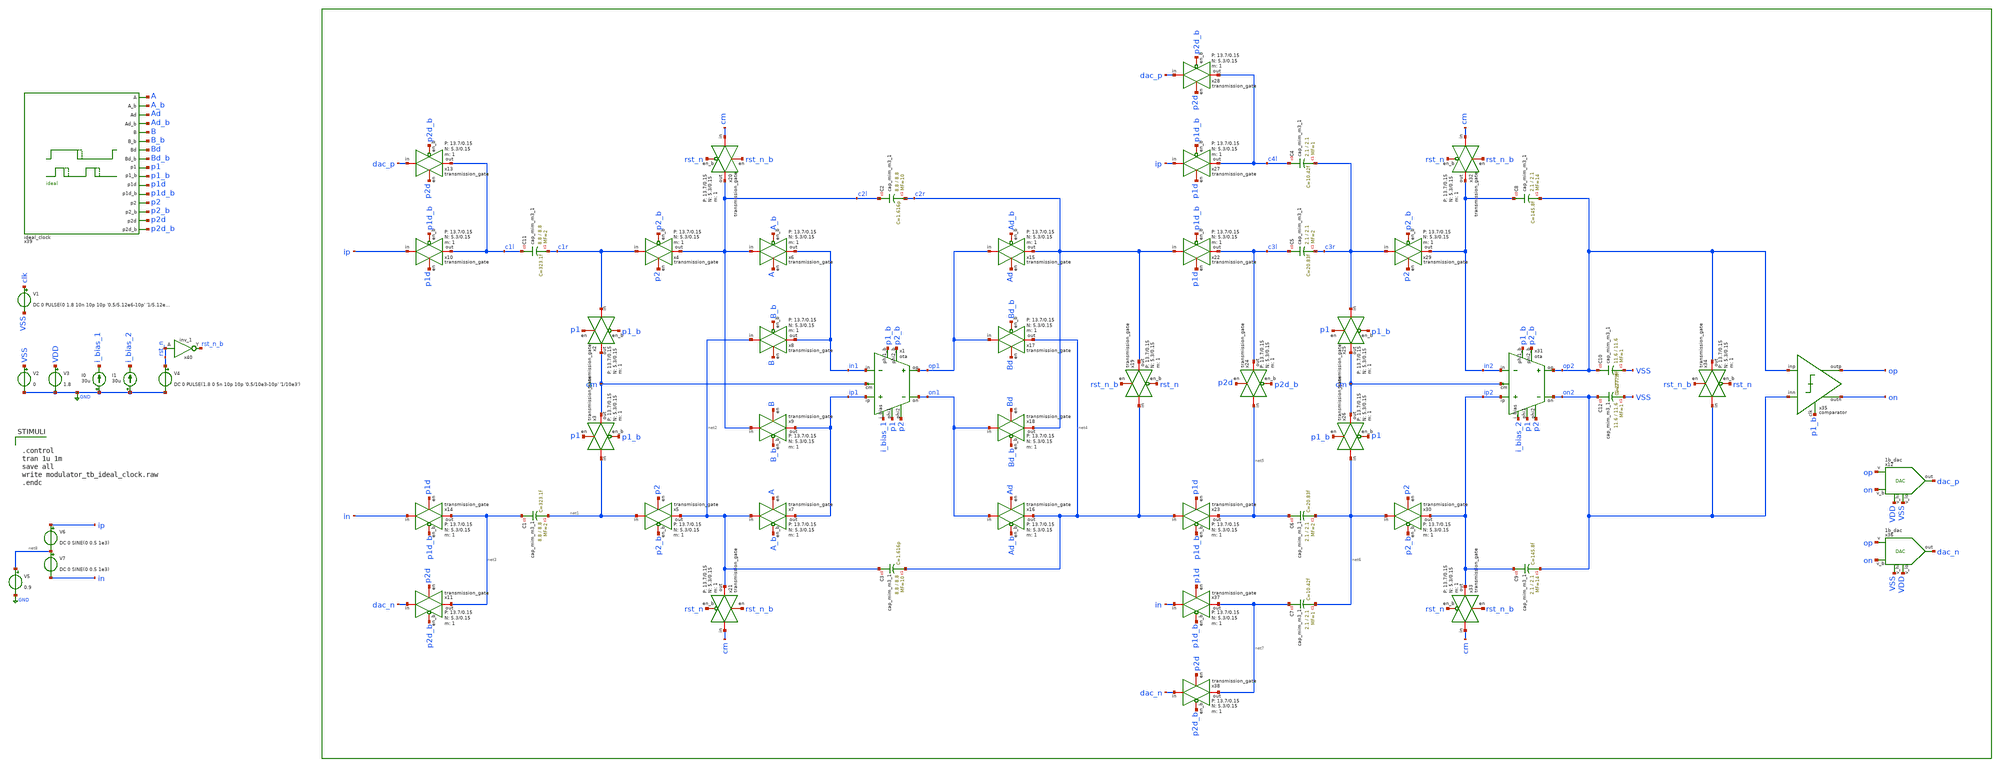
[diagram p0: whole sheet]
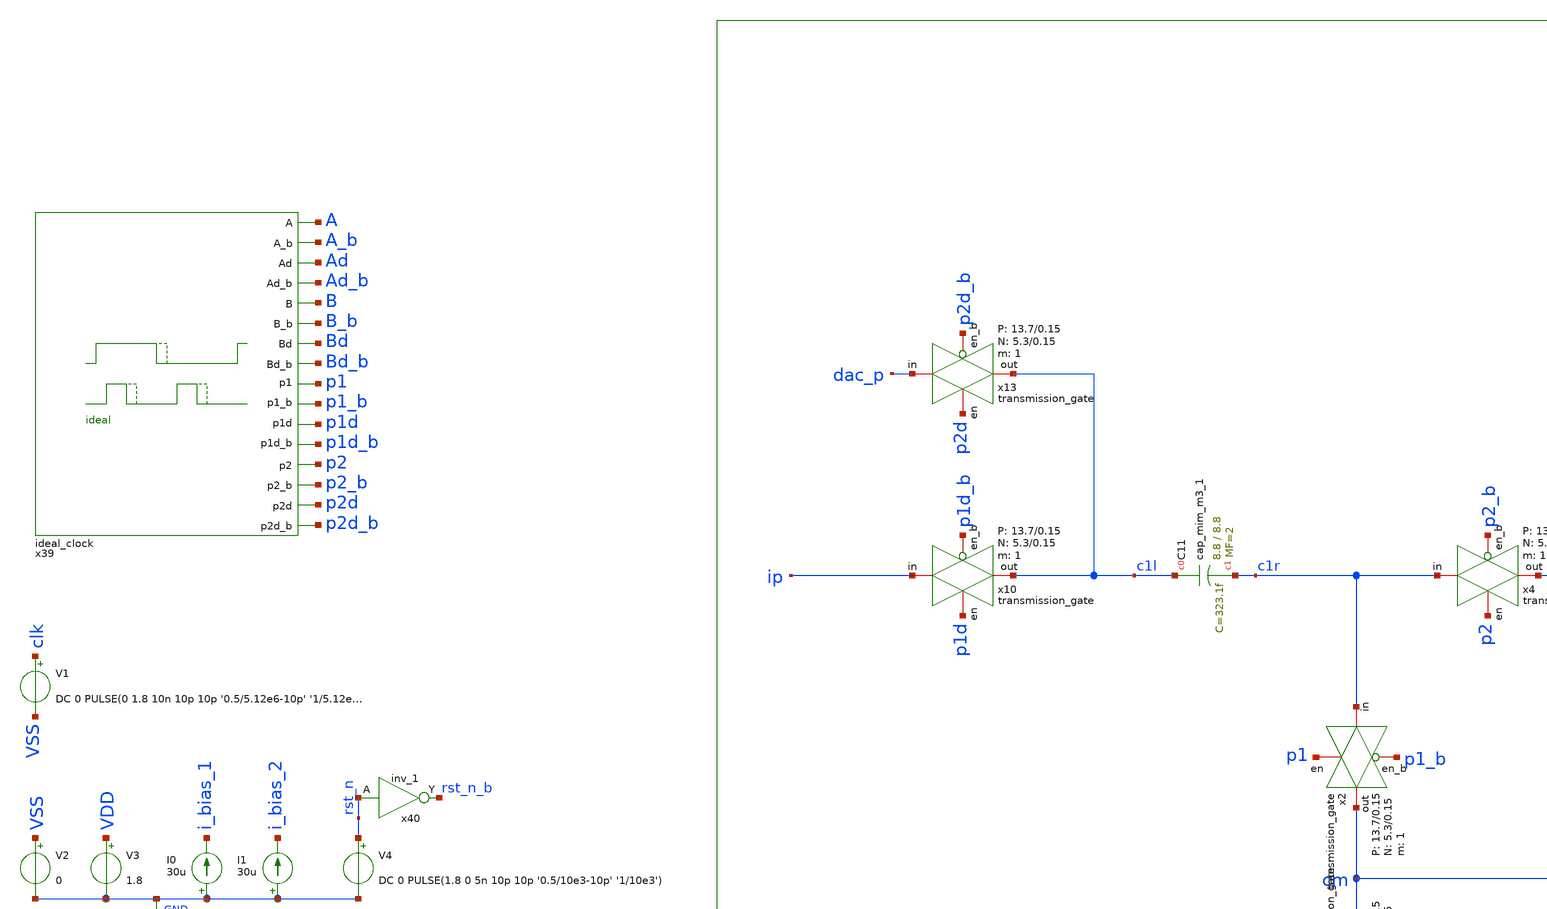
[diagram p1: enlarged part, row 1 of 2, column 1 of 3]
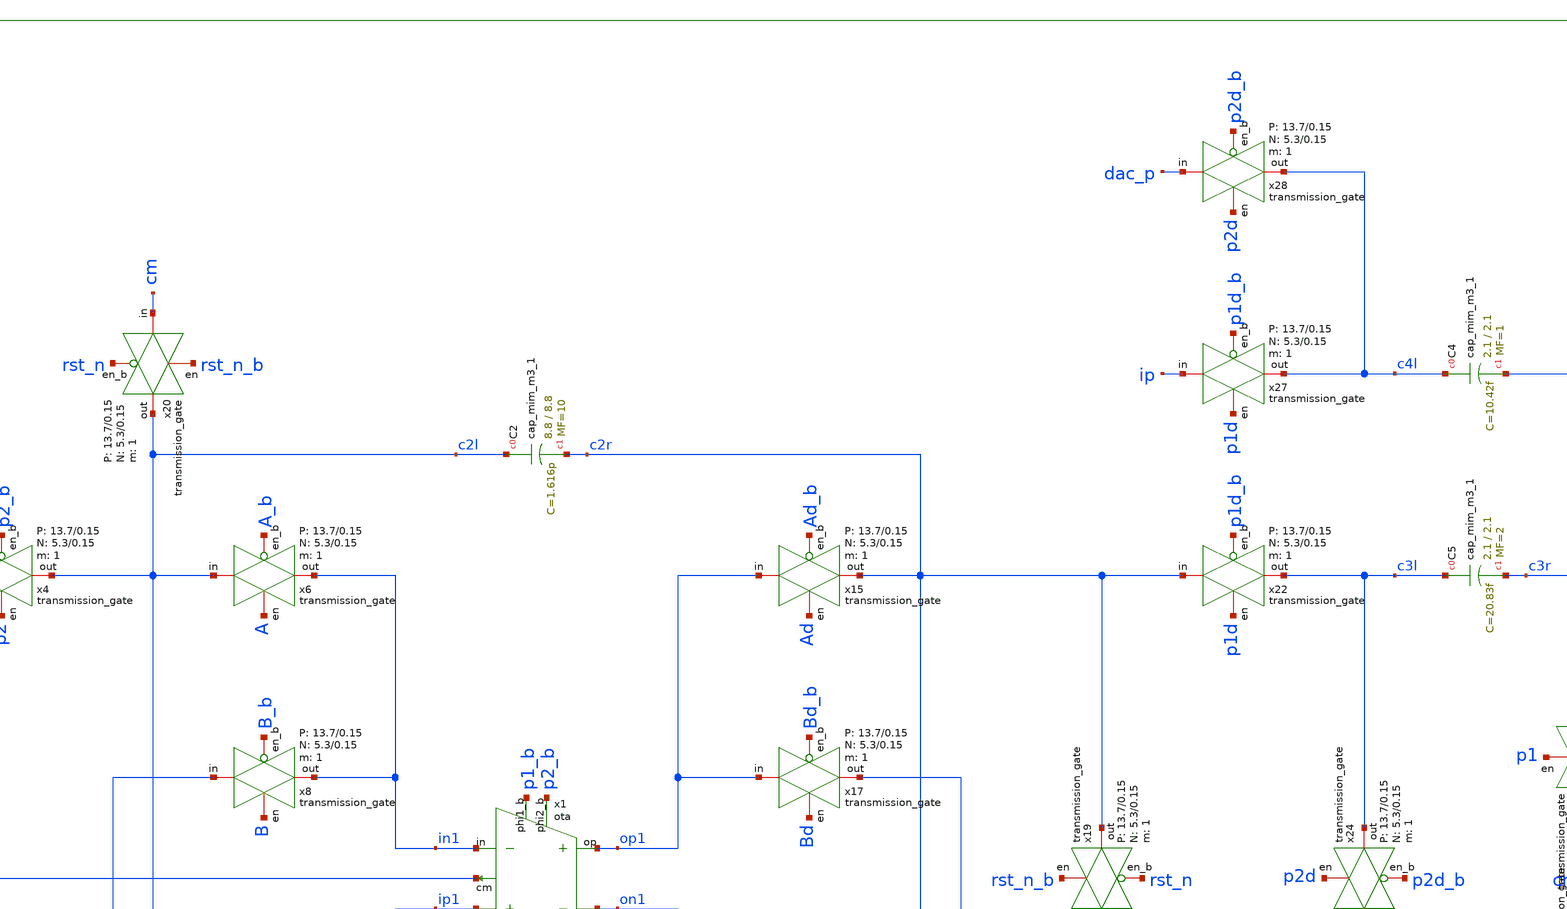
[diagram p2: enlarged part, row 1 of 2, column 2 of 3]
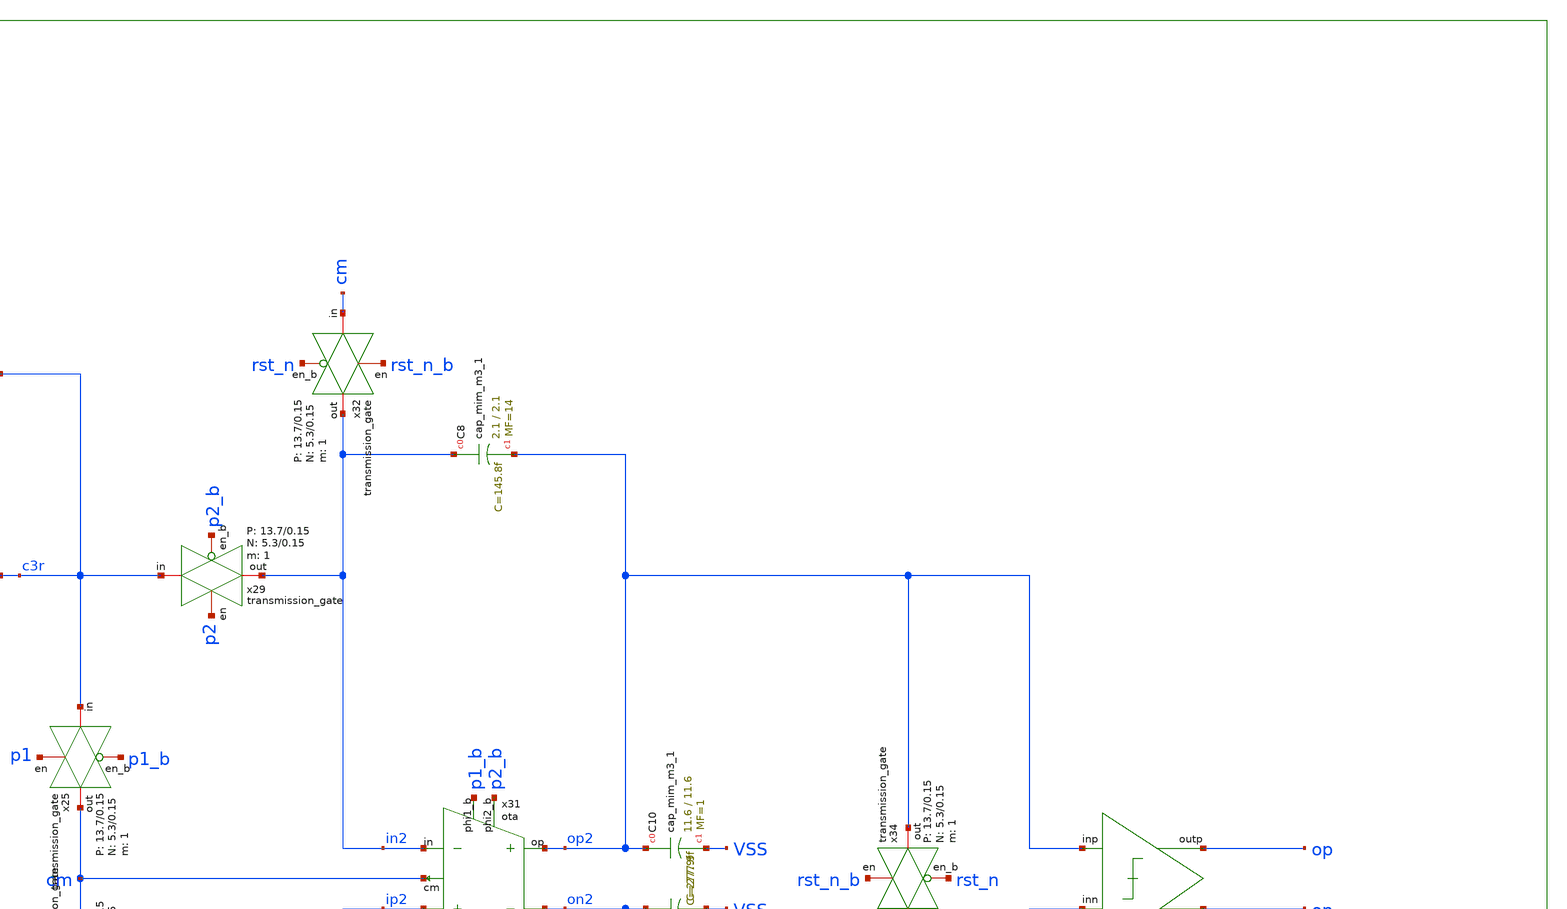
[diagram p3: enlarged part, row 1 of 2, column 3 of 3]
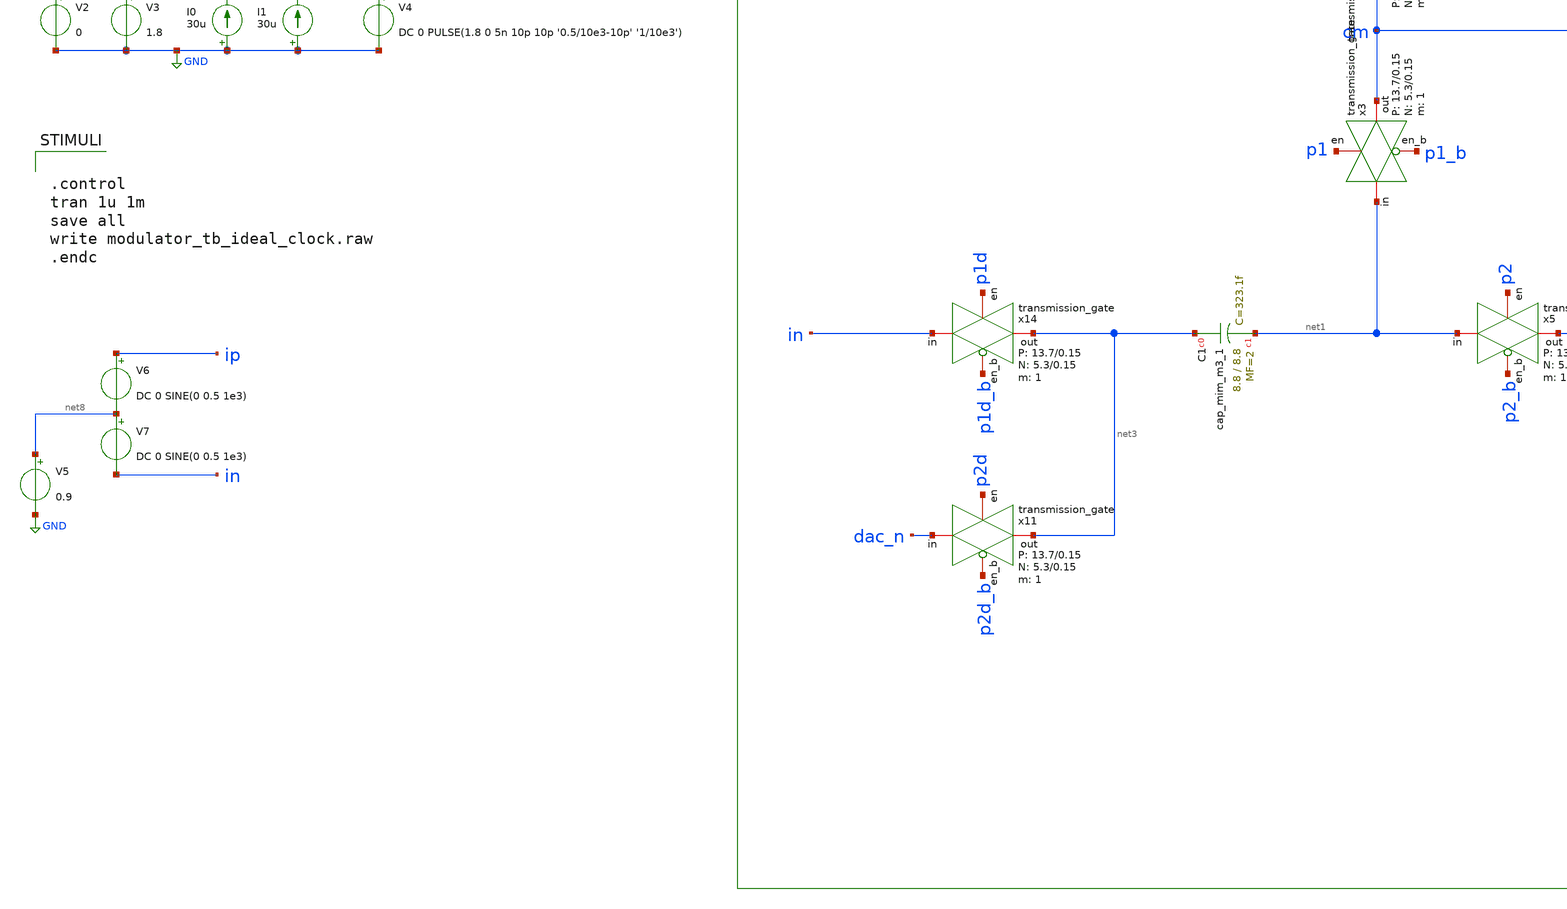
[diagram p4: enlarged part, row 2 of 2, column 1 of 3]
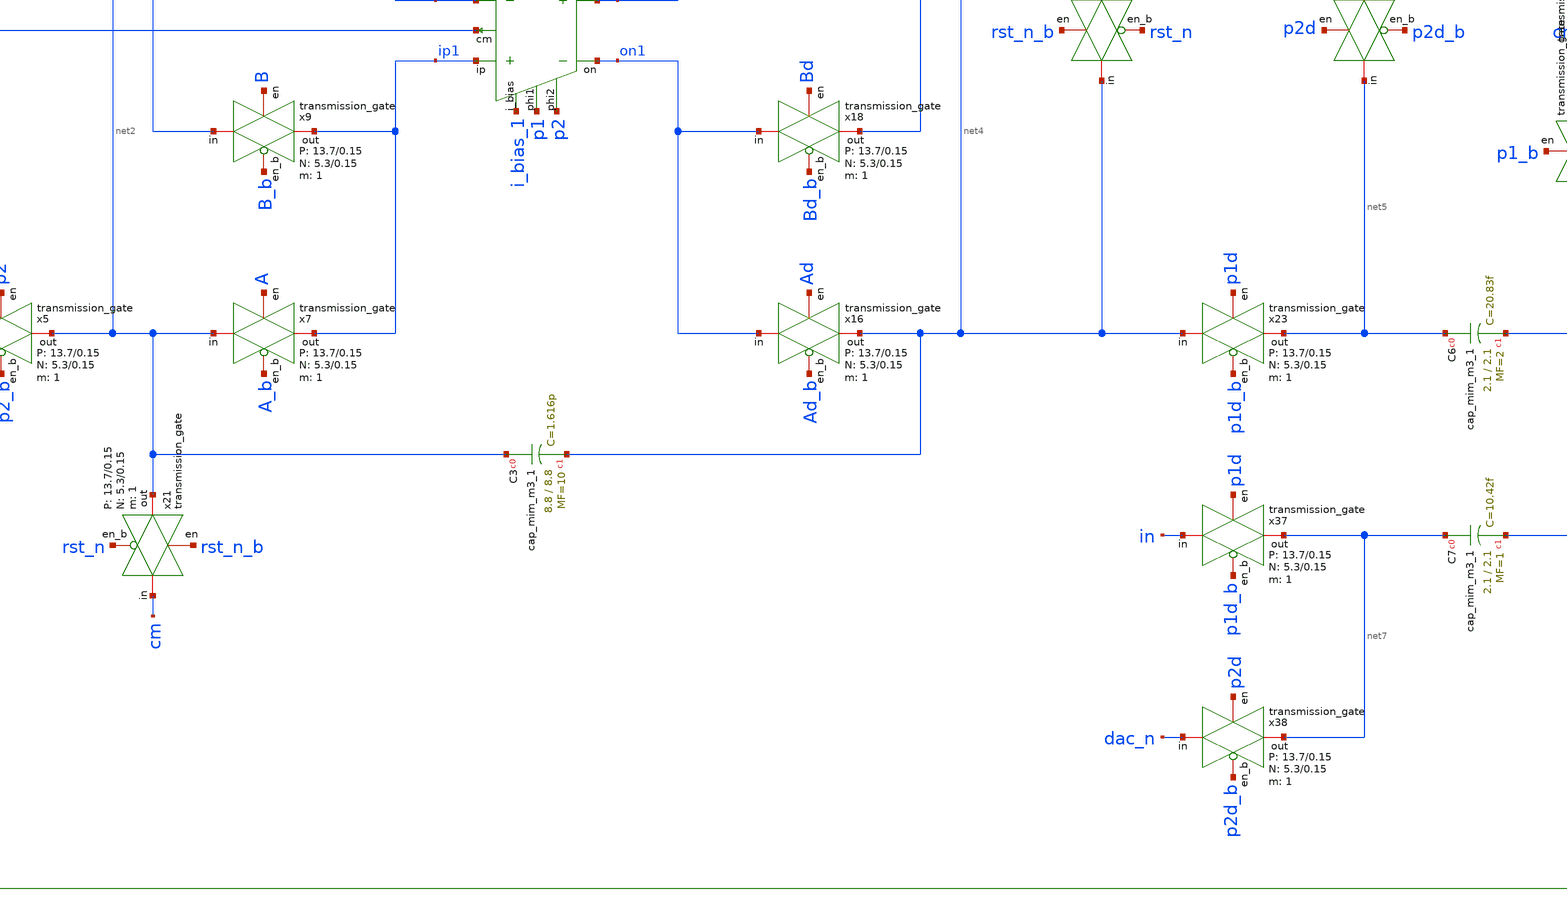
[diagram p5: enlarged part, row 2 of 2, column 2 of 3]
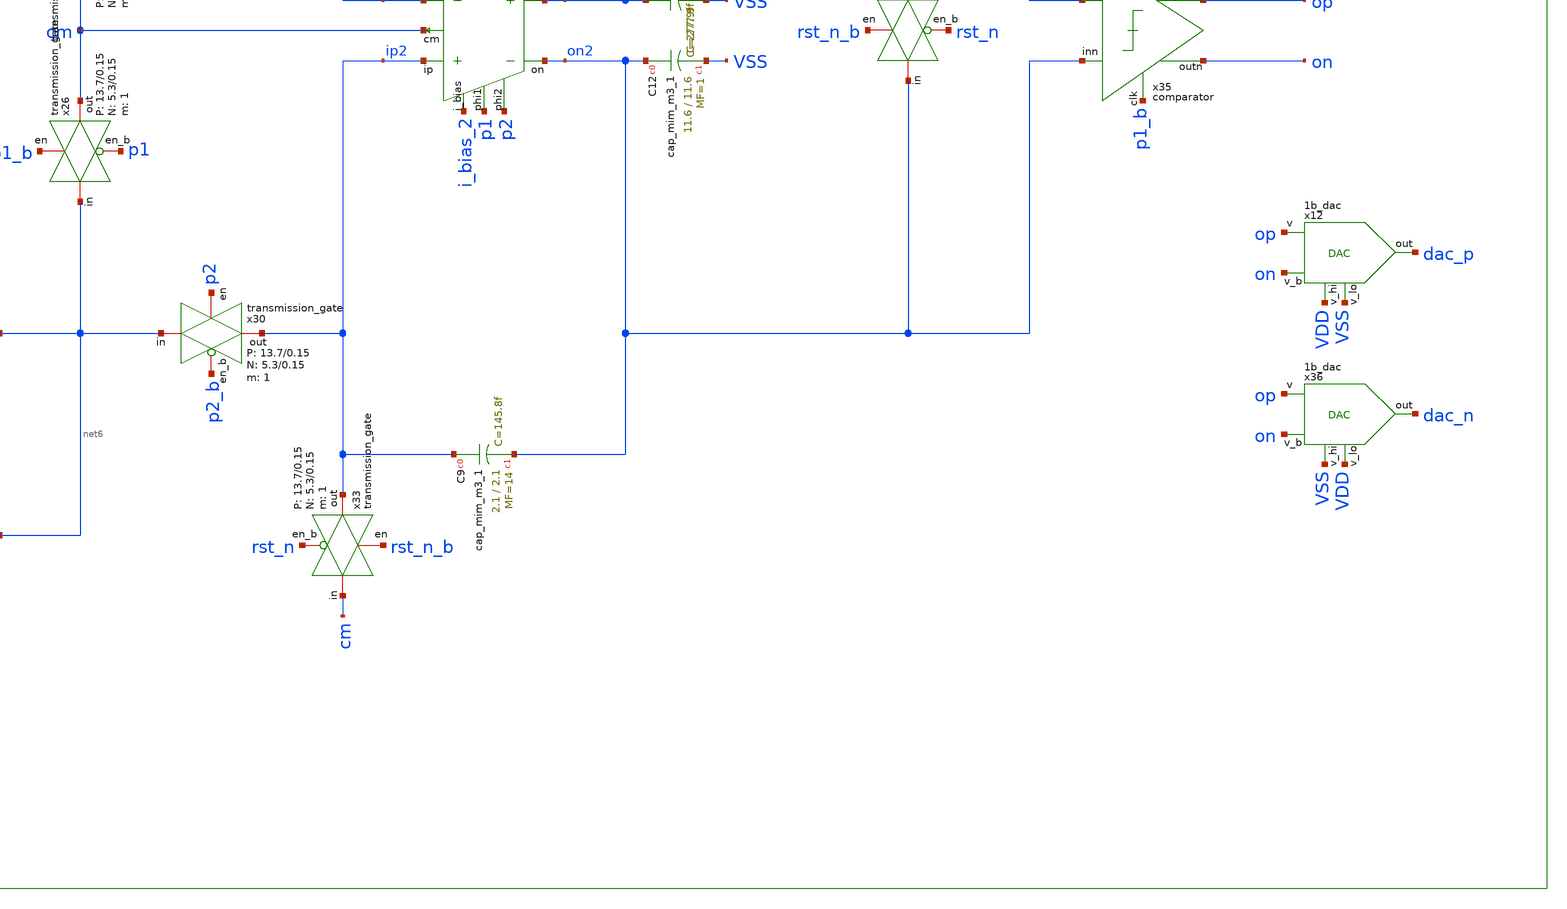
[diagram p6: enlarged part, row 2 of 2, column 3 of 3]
** sch_path: verification/schematic/modulator_tb_ideal_clock.sch
**.subckt modulator_tb_ideal_clock
x1 i_bias_1 ip1 in1 p1 p1_b p2 p2_b op1 on1 cm 50 350 VDD VSS ota
x4 c1r c2l p2 p2_b VDD VSS 1 5.3 0.15 13.7 0.15 transmission_gate
x5 net1 net2 p2 p2_b VDD VSS 1 5.3 0.15 13.7 0.15 transmission_gate
x6 c2l in1 A A_b VDD VSS 1 5.3 0.15 13.7 0.15 transmission_gate
x7 net2 ip1 A A_b VDD VSS 1 5.3 0.15 13.7 0.15 transmission_gate
x8 net2 in1 B B_b VDD VSS 1 5.3 0.15 13.7 0.15 transmission_gate
x9 c2l ip1 B B_b VDD VSS 1 5.3 0.15 13.7 0.15 transmission_gate
x2 c1r cm p1 p1_b VDD VSS 1 5.3 0.15 13.7 0.15 transmission_gate
x3 net1 cm p1 p1_b VDD VSS 1 5.3 0.15 13.7 0.15 transmission_gate
x10 ip c1l p1d p1d_b VDD VSS 1 5.3 0.15 13.7 0.15 transmission_gate
x11 dac_n net3 p2d p2d_b VDD VSS 1 5.3 0.15 13.7 0.15 transmission_gate
x12 VDD VSS op dac_p on VDD VSS 1b_dac
x13 dac_p c1l p2d p2d_b VDD VSS 1 5.3 0.15 13.7 0.15 transmission_gate
x14 in net3 p1d p1d_b VDD VSS 1 5.3 0.15 13.7 0.15 transmission_gate
x15 op1 c2r Ad Ad_b VDD VSS 1 5.3 0.15 13.7 0.15 transmission_gate
x16 on1 net4 Ad Ad_b VDD VSS 1 5.3 0.15 13.7 0.15 transmission_gate
x17 op1 net4 Bd Bd_b VDD VSS 1 5.3 0.15 13.7 0.15 transmission_gate
x18 on1 c2r Bd Bd_b VDD VSS 1 5.3 0.15 13.7 0.15 transmission_gate
x19 net4 c2r rst_n_b rst_n VDD VSS 1 5.3 0.15 13.7 0.15 transmission_gate
x20 cm c2l rst_n_b rst_n VDD VSS 1 5.3 0.15 13.7 0.15 transmission_gate
x21 cm net2 rst_n_b rst_n VDD VSS 1 5.3 0.15 13.7 0.15 transmission_gate
x22 c2r c3l p1d p1d_b VDD VSS 1 5.3 0.15 13.7 0.15 transmission_gate
x23 net4 net5 p1d p1d_b VDD VSS 1 5.3 0.15 13.7 0.15 transmission_gate
x24 net5 c3l p2d p2d_b VDD VSS 1 5.3 0.15 13.7 0.15 transmission_gate
x25 c3r cm p1 p1_b VDD VSS 1 5.3 0.15 13.7 0.15 transmission_gate
x26 net6 cm p1_b p1 VDD VSS 1 5.3 0.15 13.7 0.15 transmission_gate
x27 ip c4l p1d p1d_b VDD VSS 1 5.3 0.15 13.7 0.15 transmission_gate
x28 dac_p c4l p2d p2d_b VDD VSS 1 5.3 0.15 13.7 0.15 transmission_gate
x29 c3r in2 p2 p2_b VDD VSS 1 5.3 0.15 13.7 0.15 transmission_gate
x30 net6 ip2 p2 p2_b VDD VSS 1 5.3 0.15 13.7 0.15 transmission_gate
x31 i_bias_2 ip2 in2 p1 p1_b p2 p2_b op2 on2 cm 50 350 VDD VSS ota
x32 cm in2 rst_n_b rst_n VDD VSS 1 5.3 0.15 13.7 0.15 transmission_gate
x33 cm ip2 rst_n_b rst_n VDD VSS 1 5.3 0.15 13.7 0.15 transmission_gate
x34 on2 op2 rst_n_b rst_n VDD VSS 1 5.3 0.15 13.7 0.15 transmission_gate
x35 op2 on2 op p1_b on VDD VSS comparator
x36 VSS VDD op dac_n on VDD VSS 1b_dac
x37 in net7 p1d p1d_b VDD VSS 1 5.3 0.15 13.7 0.15 transmission_gate
x38 dac_n net7 p2d p2d_b VDD VSS 1 5.3 0.15 13.7 0.15 transmission_gate
V1 clk VSS DC 0 PULSE(0 1.8 10n 10p 10p '0.5/5.12e6-10p' '1/5.12e6')
V2 VSS GND 0
V3 VDD GND 1.8
I0 GND i_bias_1 30u
I1 GND i_bias_2 30u
V4 rst_n GND DC 0 PULSE(1.8 0 5n 10p 10p '0.5/10e3-10p' '1/10e3')
x40 rst_n GND GND VDD VDD rst_n_b sky130_fd_sc_hd__inv_1
V5 net8 GND 0.9
V6 ip net8 DC 0 SINE(0 0.5 1e3)
V7 net8 in DC 0 SINE(0 0.5 1e3)
XC11 c1l c1r sky130_fd_pr__cap_mim_m3_1 W=8.8 L=8.8 MF=2 m=2
XC1 net3 net1 sky130_fd_pr__cap_mim_m3_1 W=8.8 L=8.8 MF=2 m=2
XC2 c2l c2r sky130_fd_pr__cap_mim_m3_1 W=8.8 L=8.8 MF=10 m=10
XC3 net2 net4 sky130_fd_pr__cap_mim_m3_1 W=8.8 L=8.8 MF=10 m=10
XC4 c4l c3r sky130_fd_pr__cap_mim_m3_1 W=2.1 L=2.1 MF=1 m=1
XC5 c3l c3r sky130_fd_pr__cap_mim_m3_1 W=2.1 L=2.1 MF=2 m=2
XC6 net5 net6 sky130_fd_pr__cap_mim_m3_1 W=2.1 L=2.1 MF=2 m=2
XC7 net7 net6 sky130_fd_pr__cap_mim_m3_1 W=2.1 L=2.1 MF=1 m=1
XC8 in2 op2 sky130_fd_pr__cap_mim_m3_1 W=2.1 L=2.1 MF=14 m=14
XC9 ip2 on2 sky130_fd_pr__cap_mim_m3_1 W=2.1 L=2.1 MF=14 m=14
XC10 op2 VSS sky130_fd_pr__cap_mim_m3_1 W=11.6 L=11.6 MF=1 m=1
XC12 on2 VSS sky130_fd_pr__cap_mim_m3_1 W=11.6 L=11.6 MF=1 m=1
x39 A A_b Ad Ad_b Bd_b Bd B_b B p2 p2_b p2d p2d_b p1d_b p1d p1_b p1 10u VDD VSS ideal_clock
**** begin user architecture code

** opencircuitdesign pdks install
.lib /farmshare/home/classes/ee/372/PDKs/open_pdks_1.0.310/sky130/sky130A/libs.tech/ngspice/sky130.lib.spice tt
.inc /farmshare/home/classes/ee/372/PDKs/open_pdks_1.0.310/sky130/sky130A/libs.ref/sky130_fd_sc_hd/spice/sky130_fd_sc_hd.spice



.control
tran 1u 1m
save all
write modulator_tb_ideal_clock.raw
.endc


**** end user architecture code
**.ends
.GLOBAL GND
.end
